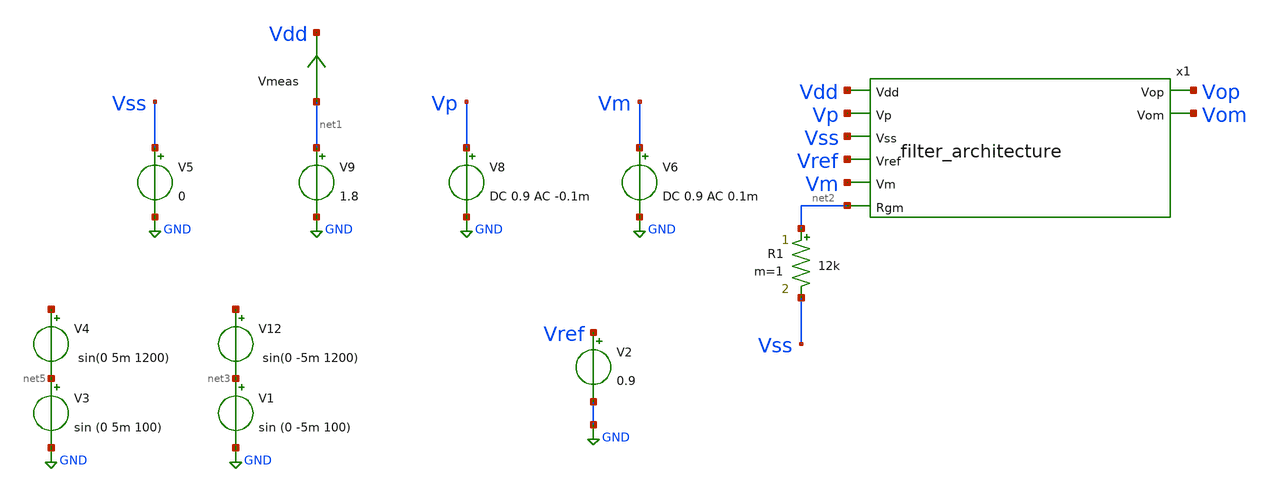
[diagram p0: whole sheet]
** sch_path: src/Bandpass_filter/testbenches/Bandpass_filter_tb.sch
**.subckt Bandpass_filter_tb
x1 Vdd Vop Vp Vss Vref Vm Vom net2 filter_architecture
V8 Vp GND DC 0.9 AC -0.1m
V6 Vm GND DC 0.9 AC 0.1m
V9 net1 GND 1.8
Vmeas net1 Vdd 0
.save i(vmeas)
V1 net3 GND sin (0 -5m 100)
V12 net4 net3 sin(0 -5m 1200)
V5 Vss GND 0
R1 net2 Vss 12k m=1
V3 net5 GND sin (0 5m 100)
V4 net6 net5 sin(0 5m 1200)
V2 Vref GND 0.9
**** begin user architecture code

** opencircuitdesign pdks install
.lib $::SKYWATER_MODELS/sky130.lib.spice tt


**** end user architecture code
**.ends

* expanding   symbol:  /foss/designs/FYP/Sky130_Design/Bandpass_filter/Src/filter_architecture.sym #
*+ of pins=8
** sym_path: src/Bandpass_filter/Src/filter_architecture.sym
** sch_path: src/Bandpass_filter/Src/filter_architecture.sch
.subckt filter_architecture Vdd Vop Vp Vss Vref Vm Vom Rgm
*.ipin Vdd
*.opin Vop
*.ipin Vss
*.ipin Vref
*.ipin Rgm
*.ipin Vp
*.ipin Vm
*.opin Vom
x1 Rgm Vop1 net2 Vdd Vref Vss Vom1 net4 Opamp_with_bias
C1 net1 net2 10n m=1
C2 net1 Vop1 10n m=1
R1 net2 Vop1 105k m=1
R2 Vm net1 36.5k m=1
R3 net1 Vref 2.37k m=1
C3 net3 net4 10n m=1
C4 net3 Vom1 10n m=1
R4 net4 Vom1 105k m=1
R5 Vp net3 36.5k m=1
R6 net3 Vref 2.37k m=1
x2 Rgm Vop net6 Vdd Vref Vss Vom net8 Opamp_with_bias
C5 net5 net6 10n m=1
C6 net5 Vop 10n m=1
R7 net6 Vop 105k m=1
R9 net5 Vref 2.37k m=1
C7 net7 net8 10n m=1
C8 net7 Vom 10n m=1
R10 net8 Vom 105k m=1
R11 Vom1 net5 36.5k m=1
R12 net7 Vref 2.37k m=1
R8 Vop1 net7 36.5k m=1
.ends


* expanding   symbol:  /foss/designs/FYP/Sky130_Design/Opamp_Design/src/Opamp_with_bias.sym # of
*+ pins=8
** sym_path: src/Opamp_Design/src/Opamp_with_bias.sym
** sch_path: src/Opamp_Design/src/Opamp_with_bias.sch
.subckt Opamp_with_bias Rgm Vop Vm Vdd Vref Vss Vom Vp
*.ipin Vdd
*.ipin Vss
*.opin Vop
*.opin Vom
*.ipin Vm
*.ipin Vp
*.ipin Vref
*.ipin Rgm
XM32 NBias PBias Vdd Vdd sky130_fd_pr__pfet_01v8_lvt L=1 W=5 nf=1 ad='int((nf+1)/2) * W/nf * 0.29' as='int((nf+2)/2) * W/nf * 0.29'
+ pd='2*int((nf+1)/2) * (W/nf + 0.29)' ps='2*int((nf+2)/2) * (W/nf + 0.29)' nrd='0.29 / W' nrs='0.29 / W'
+ sa=0 sb=0 sd=0 mult=2 m=2
XM33 NBias NBias Vss Vss sky130_fd_pr__nfet_01v8_lvt L=2 W=5 nf=1 ad='int((nf+1)/2) * W/nf * 0.29' as='int((nf+2)/2) * W/nf * 0.29'
+ pd='2*int((nf+1)/2) * (W/nf + 0.29)' ps='2*int((nf+2)/2) * (W/nf + 0.29)' nrd='0.29 / W' nrs='0.29 / W'
+ sa=0 sb=0 sd=0 mult=2 m=2
XM34 net1 PBias Vdd Vdd sky130_fd_pr__pfet_01v8_lvt L=1 W=5 nf=1 ad='int((nf+1)/2) * W/nf * 0.29' as='int((nf+2)/2) * W/nf * 0.29'
+ pd='2*int((nf+1)/2) * (W/nf + 0.29)' ps='2*int((nf+2)/2) * (W/nf + 0.29)' nrd='0.29 / W' nrs='0.29 / W'
+ sa=0 sb=0 sd=0 mult=2 m=2
XM35 net1 net1 Rgm Vss sky130_fd_pr__nfet_01v8_lvt L=1 W=10 nf=1 ad='int((nf+1)/2) * W/nf * 0.29' as='int((nf+2)/2) * W/nf * 0.29'
+ pd='2*int((nf+1)/2) * (W/nf + 0.29)' ps='2*int((nf+2)/2) * (W/nf + 0.29)' nrd='0.29 / W' nrs='0.29 / W'
+ sa=0 sb=0 sd=0 mult=2 m=2
XM36 net2 net1 Vss Vss sky130_fd_pr__nfet_01v8_lvt L=2 W=5 nf=1 ad='int((nf+1)/2) * W/nf * 0.29' as='int((nf+2)/2) * W/nf * 0.29'
+ pd='2*int((nf+1)/2) * (W/nf + 0.29)' ps='2*int((nf+2)/2) * (W/nf + 0.29)' nrd='0.29 / W' nrs='0.29 / W'
+ sa=0 sb=0 sd=0 mult=2 m=2
XM37 PBias NBias Vss Vss sky130_fd_pr__nfet_01v8_lvt L=2 W=5 nf=1 ad='int((nf+1)/2) * W/nf * 0.29' as='int((nf+2)/2) * W/nf * 0.29'
+ pd='2*int((nf+1)/2) * (W/nf + 0.29)' ps='2*int((nf+2)/2) * (W/nf + 0.29)' nrd='0.29 / W' nrs='0.29 / W'
+ sa=0 sb=0 sd=0 mult=2 m=2
XM38 PBias net2 Vdd Vdd sky130_fd_pr__pfet_01v8_lvt L=1 W=5 nf=1 ad='int((nf+1)/2) * W/nf * 0.29' as='int((nf+2)/2) * W/nf * 0.29'
+ pd='2*int((nf+1)/2) * (W/nf + 0.29)' ps='2*int((nf+2)/2) * (W/nf + 0.29)' nrd='0.29 / W' nrs='0.29 / W'
+ sa=0 sb=0 sd=0 mult=2 m=2
XM39 net2 net2 Vdd Vdd sky130_fd_pr__pfet_01v8_lvt L=1 W=5 nf=1 ad='int((nf+1)/2) * W/nf * 0.29' as='int((nf+2)/2) * W/nf * 0.29'
+ pd='2*int((nf+1)/2) * (W/nf + 0.29)' ps='2*int((nf+2)/2) * (W/nf + 0.29)' nrd='0.29 / W' nrs='0.29 / W'
+ sa=0 sb=0 sd=0 mult=2 m=2
XM40 PBias net3 NBias Vss sky130_fd_pr__nfet_01v8_lvt L=1 W=2 nf=1 ad='int((nf+1)/2) * W/nf * 0.29' as='int((nf+2)/2) * W/nf * 0.29'
+ pd='2*int((nf+1)/2) * (W/nf + 0.29)' ps='2*int((nf+2)/2) * (W/nf + 0.29)' nrd='0.29 / W' nrs='0.29 / W'
+ sa=0 sb=0 sd=0 mult=1 m=1
XM41 net3 NBias Vss Vss sky130_fd_pr__nfet_01v8_lvt L=2 W=5 nf=1 ad='int((nf+1)/2) * W/nf * 0.29' as='int((nf+2)/2) * W/nf * 0.29'
+ pd='2*int((nf+1)/2) * (W/nf + 0.29)' ps='2*int((nf+2)/2) * (W/nf + 0.29)' nrd='0.29 / W' nrs='0.29 / W'
+ sa=0 sb=0 sd=0 mult=2 m=2
XM42 net3 net3 Vdd Vdd sky130_fd_pr__pfet_01v8_lvt L=20 W=1 nf=1 ad='int((nf+1)/2) * W/nf * 0.29' as='int((nf+2)/2) * W/nf * 0.29'
+ pd='2*int((nf+1)/2) * (W/nf + 0.29)' ps='2*int((nf+2)/2) * (W/nf + 0.29)' nrd='0.29 / W' nrs='0.29 / W'
+ sa=0 sb=0 sd=0 mult=2 m=2
XM43 net4 PBias Vdd Vdd sky130_fd_pr__pfet_01v8_lvt L=1 W=5 nf=1 ad='int((nf+1)/2) * W/nf * 0.29' as='int((nf+2)/2) * W/nf * 0.29'
+ pd='2*int((nf+1)/2) * (W/nf + 0.29)' ps='2*int((nf+2)/2) * (W/nf + 0.29)' nrd='0.29 / W' nrs='0.29 / W'
+ sa=0 sb=0 sd=0 mult=2 m=2
XM44 net5 PBias Vdd Vdd sky130_fd_pr__pfet_01v8_lvt L=1 W=5 nf=1 ad='int((nf+1)/2) * W/nf * 0.29' as='int((nf+2)/2) * W/nf * 0.29'
+ pd='2*int((nf+1)/2) * (W/nf + 0.29)' ps='2*int((nf+2)/2) * (W/nf + 0.29)' nrd='0.29 / W' nrs='0.29 / W'
+ sa=0 sb=0 sd=0 mult=2 m=2
XM45 net6 PBias Vdd Vdd sky130_fd_pr__pfet_01v8_lvt L=1 W=5 nf=1 ad='int((nf+1)/2) * W/nf * 0.29' as='int((nf+2)/2) * W/nf * 0.29'
+ pd='2*int((nf+1)/2) * (W/nf + 0.29)' ps='2*int((nf+2)/2) * (W/nf + 0.29)' nrd='0.29 / W' nrs='0.29 / W'
+ sa=0 sb=0 sd=0 mult=2 m=2
XM54 net7 PBias Vdd Vdd sky130_fd_pr__pfet_01v8_lvt L=1 W=5 nf=1 ad='int((nf+1)/2) * W/nf * 0.29' as='int((nf+2)/2) * W/nf * 0.29'
+ pd='2*int((nf+1)/2) * (W/nf + 0.29)' ps='2*int((nf+2)/2) * (W/nf + 0.29)' nrd='0.29 / W' nrs='0.29 / W'
+ sa=0 sb=0 sd=0 mult=2 m=2
XC1 Vop1 Vom sky130_fd_pr__cap_mim_m3_1 W=10 L=10 MF=5 m=5
XC2 Vom1 Vop sky130_fd_pr__cap_mim_m3_1 W=10 L=10 MF=5 m=5
x1 net6 net5 net4 Vm Vp Vss Vdd Vref Vop1 Vom1 Diff_opamp
x2 Vref net7 Vop1 Vom1 Vss Vdd Vop Vom Common_source_stage
.ends


* expanding   symbol:  /foss/designs/FYP/Sky130_Design/Opamp_Design/src/Diff_opamp.sym # of pins=10
** sym_path: src/Opamp_Design/src/Diff_opamp.sym
** sch_path: src/Opamp_Design/src/Diff_opamp.sch
.subckt Diff_opamp Vbias3 Vbias2 Vbias1 Vm Vp Vss Vdd Vref Vop Vom
*.ipin Vss
*.opin Vop
*.ipin Vdd
*.ipin Vp
*.ipin Vm
*.ipin Vref
*.opin Vom
*.ipin Vbias1
*.ipin Vbias2
*.ipin Vbias3
XM5 Vtest2 Vm net2 Vss sky130_fd_pr__nfet_01v8_lvt L=4 W=4 nf=1 ad='int((nf+1)/2) * W/nf * 0.29' as='int((nf+2)/2) * W/nf * 0.29'
+ pd='2*int((nf+1)/2) * (W/nf + 0.29)' ps='2*int((nf+2)/2) * (W/nf + 0.29)' nrd='0.29 / W' nrs='0.29 / W'
+ sa=0 sb=0 sd=0 mult=2 m=2
XM6 net1 Vp net2 Vss sky130_fd_pr__nfet_01v8_lvt L=4 W=4 nf=1 ad='int((nf+1)/2) * W/nf * 0.29' as='int((nf+2)/2) * W/nf * 0.29'
+ pd='2*int((nf+1)/2) * (W/nf + 0.29)' ps='2*int((nf+2)/2) * (W/nf + 0.29)' nrd='0.29 / W' nrs='0.29 / W'
+ sa=0 sb=0 sd=0 mult=2 m=2
XM11 Vop Vbias Vtest2 Vdd sky130_fd_pr__pfet_01v8_lvt L=5 W=2 nf=1 ad='int((nf+1)/2) * W/nf * 0.29' as='int((nf+2)/2) * W/nf * 0.29'
+ pd='2*int((nf+1)/2) * (W/nf + 0.29)' ps='2*int((nf+2)/2) * (W/nf + 0.29)' nrd='0.29 / W' nrs='0.29 / W'
+ sa=0 sb=0 sd=0 mult=2 m=2
XM12 Vom Vbias net1 Vdd sky130_fd_pr__pfet_01v8_lvt L=5 W=2 nf=1 ad='int((nf+1)/2) * W/nf * 0.29' as='int((nf+2)/2) * W/nf * 0.29'
+ pd='2*int((nf+1)/2) * (W/nf + 0.29)' ps='2*int((nf+2)/2) * (W/nf + 0.29)' nrd='0.29 / W' nrs='0.29 / W'
+ sa=0 sb=0 sd=0 mult=2 m=2
XM13 Vtest2 Vout Vdd Vdd sky130_fd_pr__pfet_01v8_lvt L=5 W=2 nf=1 ad='int((nf+1)/2) * W/nf * 0.29' as='int((nf+2)/2) * W/nf * 0.29'
+ pd='2*int((nf+1)/2) * (W/nf + 0.29)' ps='2*int((nf+2)/2) * (W/nf + 0.29)' nrd='0.29 / W' nrs='0.29 / W'
+ sa=0 sb=0 sd=0 mult=4 m=4
XM14 net1 Vout Vdd Vdd sky130_fd_pr__pfet_01v8_lvt L=5 W=2 nf=1 ad='int((nf+1)/2) * W/nf * 0.29' as='int((nf+2)/2) * W/nf * 0.29'
+ pd='2*int((nf+1)/2) * (W/nf + 0.29)' ps='2*int((nf+2)/2) * (W/nf + 0.29)' nrd='0.29 / W' nrs='0.29 / W'
+ sa=0 sb=0 sd=0 mult=4 m=4
XM19 net2 Vbias2 net3 Vss sky130_fd_pr__nfet_01v8_lvt L=1 W=1 nf=1 ad='int((nf+1)/2) * W/nf * 0.29' as='int((nf+2)/2) * W/nf * 0.29'
+ pd='2*int((nf+1)/2) * (W/nf + 0.29)' ps='2*int((nf+2)/2) * (W/nf + 0.29)' nrd='0.29 / W' nrs='0.29 / W'
+ sa=0 sb=0 sd=0 mult=2 m=2
XM1 net3 Vbias1 Vss Vss sky130_fd_pr__nfet_01v8_lvt L=10 W=1 nf=1 ad='int((nf+1)/2) * W/nf * 0.29' as='int((nf+2)/2) * W/nf * 0.29'
+ pd='2*int((nf+1)/2) * (W/nf + 0.29)' ps='2*int((nf+2)/2) * (W/nf + 0.29)' nrd='0.29 / W' nrs='0.29 / W'
+ sa=0 sb=0 sd=0 mult=2 m=2
XM2 net4 Vbias1 Vss Vss sky130_fd_pr__nfet_01v8_lvt L=10 W=1 nf=1 ad='int((nf+1)/2) * W/nf * 0.29' as='int((nf+2)/2) * W/nf * 0.29'
+ pd='2*int((nf+1)/2) * (W/nf + 0.29)' ps='2*int((nf+2)/2) * (W/nf + 0.29)' nrd='0.29 / W' nrs='0.29 / W'
+ sa=0 sb=0 sd=0 mult=2 m=2
XM3 net2 Vbias2 net4 Vss sky130_fd_pr__nfet_01v8_lvt L=1 W=1 nf=1 ad='int((nf+1)/2) * W/nf * 0.29' as='int((nf+2)/2) * W/nf * 0.29'
+ pd='2*int((nf+1)/2) * (W/nf + 0.29)' ps='2*int((nf+2)/2) * (W/nf + 0.29)' nrd='0.29 / W' nrs='0.29 / W'
+ sa=0 sb=0 sd=0 mult=2 m=2
XM4 Vop Vbias2 net5 Vss sky130_fd_pr__nfet_01v8_lvt L=1 W=1 nf=1 ad='int((nf+1)/2) * W/nf * 0.29' as='int((nf+2)/2) * W/nf * 0.29'
+ pd='2*int((nf+1)/2) * (W/nf + 0.29)' ps='2*int((nf+2)/2) * (W/nf + 0.29)' nrd='0.29 / W' nrs='0.29 / W'
+ sa=0 sb=0 sd=0 mult=2 m=2
XM7 net5 Vbias1 Vss Vss sky130_fd_pr__nfet_01v8_lvt L=10 W=1 nf=1 ad='int((nf+1)/2) * W/nf * 0.29' as='int((nf+2)/2) * W/nf * 0.29'
+ pd='2*int((nf+1)/2) * (W/nf + 0.29)' ps='2*int((nf+2)/2) * (W/nf + 0.29)' nrd='0.29 / W' nrs='0.29 / W'
+ sa=0 sb=0 sd=0 mult=2 m=2
XM8 Vom Vbias2 net6 Vss sky130_fd_pr__nfet_01v8_lvt L=1 W=1 nf=1 ad='int((nf+1)/2) * W/nf * 0.29' as='int((nf+2)/2) * W/nf * 0.29'
+ pd='2*int((nf+1)/2) * (W/nf + 0.29)' ps='2*int((nf+2)/2) * (W/nf + 0.29)' nrd='0.29 / W' nrs='0.29 / W'
+ sa=0 sb=0 sd=0 mult=2 m=2
XM9 net6 Vbias1 Vss Vss sky130_fd_pr__nfet_01v8_lvt L=10 W=1 nf=1 ad='int((nf+1)/2) * W/nf * 0.29' as='int((nf+2)/2) * W/nf * 0.29'
+ pd='2*int((nf+1)/2) * (W/nf + 0.29)' ps='2*int((nf+2)/2) * (W/nf + 0.29)' nrd='0.29 / W' nrs='0.29 / W'
+ sa=0 sb=0 sd=0 mult=2 m=2
XM10 Vout Vref net8 Vss sky130_fd_pr__nfet_01v8_lvt L=20 W=5 nf=1 ad='int((nf+1)/2) * W/nf * 0.29' as='int((nf+2)/2) * W/nf * 0.29'
+ pd='2*int((nf+1)/2) * (W/nf + 0.29)' ps='2*int((nf+2)/2) * (W/nf + 0.29)' nrd='0.29 / W' nrs='0.29 / W'
+ sa=0 sb=0 sd=0 mult=2 m=2
XM17 net9 Vop net8 Vss sky130_fd_pr__nfet_01v8_lvt L=20 W=5 nf=1 ad='int((nf+1)/2) * W/nf * 0.29' as='int((nf+2)/2) * W/nf * 0.29'
+ pd='2*int((nf+1)/2) * (W/nf + 0.29)' ps='2*int((nf+2)/2) * (W/nf + 0.29)' nrd='0.29 / W' nrs='0.29 / W'
+ sa=0 sb=0 sd=0 mult=2 m=2
XM18 net9 Vom net7 Vss sky130_fd_pr__nfet_01v8_lvt L=20 W=5 nf=1 ad='int((nf+1)/2) * W/nf * 0.29' as='int((nf+2)/2) * W/nf * 0.29'
+ pd='2*int((nf+1)/2) * (W/nf + 0.29)' ps='2*int((nf+2)/2) * (W/nf + 0.29)' nrd='0.29 / W' nrs='0.29 / W'
+ sa=0 sb=0 sd=0 mult=2 m=2
XM22 net7 Vbias1 Vss Vss sky130_fd_pr__nfet_01v8_lvt L=20 W=1 nf=1 ad='int((nf+1)/2) * W/nf * 0.29' as='int((nf+2)/2) * W/nf * 0.29'
+ pd='2*int((nf+1)/2) * (W/nf + 0.29)' ps='2*int((nf+2)/2) * (W/nf + 0.29)' nrd='0.29 / W' nrs='0.29 / W'
+ sa=0 sb=0 sd=0 mult=2 m=2
XM20 net9 net9 Vdd Vdd sky130_fd_pr__pfet_01v8_lvt L=10 W=1 nf=1 ad='int((nf+1)/2) * W/nf * 0.29' as='int((nf+2)/2) * W/nf * 0.29'
+ pd='2*int((nf+1)/2) * (W/nf + 0.29)' ps='2*int((nf+2)/2) * (W/nf + 0.29)' nrd='0.29 / W' nrs='0.29 / W'
+ sa=0 sb=0 sd=0 mult=2 m=2
XM21 Vout net9 Vdd Vdd sky130_fd_pr__pfet_01v8_lvt L=10 W=1 nf=1 ad='int((nf+1)/2) * W/nf * 0.29' as='int((nf+2)/2) * W/nf * 0.29'
+ pd='2*int((nf+1)/2) * (W/nf + 0.29)' ps='2*int((nf+2)/2) * (W/nf + 0.29)' nrd='0.29 / W' nrs='0.29 / W'
+ sa=0 sb=0 sd=0 mult=2 m=2
XM15 net8 Vbias1 Vss Vss sky130_fd_pr__nfet_01v8_lvt L=20 W=1 nf=1 ad='int((nf+1)/2) * W/nf * 0.29' as='int((nf+2)/2) * W/nf * 0.29'
+ pd='2*int((nf+1)/2) * (W/nf + 0.29)' ps='2*int((nf+2)/2) * (W/nf + 0.29)' nrd='0.29 / W' nrs='0.29 / W'
+ sa=0 sb=0 sd=0 mult=2 m=2
XM16 Vout Vref net7 Vss sky130_fd_pr__nfet_01v8_lvt L=20 W=5 nf=1 ad='int((nf+1)/2) * W/nf * 0.29' as='int((nf+2)/2) * W/nf * 0.29'
+ pd='2*int((nf+1)/2) * (W/nf + 0.29)' ps='2*int((nf+2)/2) * (W/nf + 0.29)' nrd='0.29 / W' nrs='0.29 / W'
+ sa=0 sb=0 sd=0 mult=2 m=2
XM46 Vbias1 Vbias1 Vss Vss sky130_fd_pr__nfet_01v8_lvt L=2 W=1 nf=1 ad='int((nf+1)/2) * W/nf * 0.29'
+ as='int((nf+2)/2) * W/nf * 0.29' pd='2*int((nf+1)/2) * (W/nf + 0.29)' ps='2*int((nf+2)/2) * (W/nf + 0.29)'
+ nrd='0.29 / W' nrs='0.29 / W' sa=0 sb=0 sd=0 mult=2 m=2
XM47 Vbias2 Vbias2 Vss Vss sky130_fd_pr__nfet_01v8_lvt L=5 W=0.6 nf=1 ad='int((nf+1)/2) * W/nf * 0.29'
+ as='int((nf+2)/2) * W/nf * 0.29' pd='2*int((nf+1)/2) * (W/nf + 0.29)' ps='2*int((nf+2)/2) * (W/nf + 0.29)'
+ nrd='0.29 / W' nrs='0.29 / W' sa=0 sb=0 sd=0 mult=2 m=2
XM23 Vbias3 Vbias3 Vss Vss sky130_fd_pr__nfet_01v8_lvt L=1 W=0.6 nf=1 ad='int((nf+1)/2) * W/nf * 0.29'
+ as='int((nf+2)/2) * W/nf * 0.29' pd='2*int((nf+1)/2) * (W/nf + 0.29)' ps='2*int((nf+2)/2) * (W/nf + 0.29)'
+ nrd='0.29 / W' nrs='0.29 / W' sa=0 sb=0 sd=0 mult=2 m=2
XM24 Vbias Vbias3 Vss Vss sky130_fd_pr__nfet_01v8_lvt L=1 W=0.6 nf=1 ad='int((nf+1)/2) * W/nf * 0.29'
+ as='int((nf+2)/2) * W/nf * 0.29' pd='2*int((nf+1)/2) * (W/nf + 0.29)' ps='2*int((nf+2)/2) * (W/nf + 0.29)'
+ nrd='0.29 / W' nrs='0.29 / W' sa=0 sb=0 sd=0 mult=2 m=2
XM25 Vbias Vbias Vdd Vdd sky130_fd_pr__pfet_01v8_lvt L=10 W=1.5 nf=1 ad='int((nf+1)/2) * W/nf * 0.29'
+ as='int((nf+2)/2) * W/nf * 0.29' pd='2*int((nf+1)/2) * (W/nf + 0.29)' ps='2*int((nf+2)/2) * (W/nf + 0.29)'
+ nrd='0.29 / W' nrs='0.29 / W' sa=0 sb=0 sd=0 mult=2 m=2
.ends


* expanding   symbol:  /foss/designs/FYP/Sky130_Design/Opamp_Design/src/Common_source_stage.sym # of
*+ pins=8
** sym_path: src/Opamp_Design/src/Common_source_stage.sym
** sch_path: src/Opamp_Design/src/Common_source_stage.sch
.subckt Common_source_stage Vref Vbias Vomin Vopin Vss Vdd Vop Vom
*.ipin Vdd
*.opin Vop
*.ipin Vss
*.opin Vom
*.ipin Vopin
*.ipin Vomin
*.ipin Vbias
*.ipin Vref
XM9 Vop Vopin Vdd Vdd sky130_fd_pr__pfet_01v8_lvt L=1 W=2 nf=1 ad='int((nf+1)/2) * W/nf * 0.29' as='int((nf+2)/2) * W/nf * 0.29'
+ pd='2*int((nf+1)/2) * (W/nf + 0.29)' ps='2*int((nf+2)/2) * (W/nf + 0.29)' nrd='0.29 / W' nrs='0.29 / W'
+ sa=0 sb=0 sd=0 mult=9 m=9
XM4 Vom Vomin Vdd Vdd sky130_fd_pr__pfet_01v8_lvt L=1 W=2 nf=1 ad='int((nf+1)/2) * W/nf * 0.29' as='int((nf+2)/2) * W/nf * 0.29'
+ pd='2*int((nf+1)/2) * (W/nf + 0.29)' ps='2*int((nf+2)/2) * (W/nf + 0.29)' nrd='0.29 / W' nrs='0.29 / W'
+ sa=0 sb=0 sd=0 mult=9 m=9
XM2 Vop Vout Vss Vss sky130_fd_pr__nfet_01v8_lvt L=1 W=1 nf=1 ad='int((nf+1)/2) * W/nf * 0.29' as='int((nf+2)/2) * W/nf * 0.29'
+ pd='2*int((nf+1)/2) * (W/nf + 0.29)' ps='2*int((nf+2)/2) * (W/nf + 0.29)' nrd='0.29 / W' nrs='0.29 / W'
+ sa=0 sb=0 sd=0 mult=9 m=9
XM1 Vom Vout Vss Vss sky130_fd_pr__nfet_01v8_lvt L=1 W=1 nf=1 ad='int((nf+1)/2) * W/nf * 0.29' as='int((nf+2)/2) * W/nf * 0.29'
+ pd='2*int((nf+1)/2) * (W/nf + 0.29)' ps='2*int((nf+2)/2) * (W/nf + 0.29)' nrd='0.29 / W' nrs='0.29 / W'
+ sa=0 sb=0 sd=0 mult=9 m=9
XM3 net1 Vbiasp Vdd Vdd sky130_fd_pr__pfet_01v8_lvt L=5 W=1 nf=1 ad='int((nf+1)/2) * W/nf * 0.29' as='int((nf+2)/2) * W/nf * 0.29'
+ pd='2*int((nf+1)/2) * (W/nf + 0.29)' ps='2*int((nf+2)/2) * (W/nf + 0.29)' nrd='0.29 / W' nrs='0.29 / W'
+ sa=0 sb=0 sd=0 mult=2 m=2
XM7 Vtest Vcm net1 Vdd sky130_fd_pr__pfet_01v8_lvt L=10 W=1 nf=1 ad='int((nf+1)/2) * W/nf * 0.29' as='int((nf+2)/2) * W/nf * 0.29'
+ pd='2*int((nf+1)/2) * (W/nf + 0.29)' ps='2*int((nf+2)/2) * (W/nf + 0.29)' nrd='0.29 / W' nrs='0.29 / W'
+ sa=0 sb=0 sd=0 mult=2 m=2
XM8 Vout Vref net1 Vdd sky130_fd_pr__pfet_01v8_lvt L=10 W=1 nf=1 ad='int((nf+1)/2) * W/nf * 0.29' as='int((nf+2)/2) * W/nf * 0.29'
+ pd='2*int((nf+1)/2) * (W/nf + 0.29)' ps='2*int((nf+2)/2) * (W/nf + 0.29)' nrd='0.29 / W' nrs='0.29 / W'
+ sa=0 sb=0 sd=0 mult=2 m=2
XM5 Vtest Vtest Vss Vss sky130_fd_pr__nfet_01v8_lvt L=20 W=0.5 nf=1 ad='int((nf+1)/2) * W/nf * 0.29'
+ as='int((nf+2)/2) * W/nf * 0.29' pd='2*int((nf+1)/2) * (W/nf + 0.29)' ps='2*int((nf+2)/2) * (W/nf + 0.29)'
+ nrd='0.29 / W' nrs='0.29 / W' sa=0 sb=0 sd=0 mult=2 m=2
XM6 Vout Vtest Vss Vss sky130_fd_pr__nfet_01v8_lvt L=20 W=0.5 nf=1 ad='int((nf+1)/2) * W/nf * 0.29' as='int((nf+2)/2) * W/nf * 0.29'
+ pd='2*int((nf+1)/2) * (W/nf + 0.29)' ps='2*int((nf+2)/2) * (W/nf + 0.29)' nrd='0.29 / W' nrs='0.29 / W'
+ sa=0 sb=0 sd=0 mult=2 m=2
x1 Vop Vcm res_pack
x2 Vcm Vom res_pack
XM10 Vbias Vbias Vss Vss sky130_fd_pr__nfet_01v8_lvt L=1 W=0.6 nf=1 ad='int((nf+1)/2) * W/nf * 0.29'
+ as='int((nf+2)/2) * W/nf * 0.29' pd='2*int((nf+1)/2) * (W/nf + 0.29)' ps='2*int((nf+2)/2) * (W/nf + 0.29)'
+ nrd='0.29 / W' nrs='0.29 / W' sa=0 sb=0 sd=0 mult=2 m=2
XM11 Vbiasp Vbias Vss Vss sky130_fd_pr__nfet_01v8_lvt L=1 W=0.6 nf=1 ad='int((nf+1)/2) * W/nf * 0.29'
+ as='int((nf+2)/2) * W/nf * 0.29' pd='2*int((nf+1)/2) * (W/nf + 0.29)' ps='2*int((nf+2)/2) * (W/nf + 0.29)'
+ nrd='0.29 / W' nrs='0.29 / W' sa=0 sb=0 sd=0 mult=2 m=2
XM12 Vbiasp Vbiasp Vdd Vdd sky130_fd_pr__pfet_01v8_lvt L=1 W=6 nf=1 ad='int((nf+1)/2) * W/nf * 0.29'
+ as='int((nf+2)/2) * W/nf * 0.29' pd='2*int((nf+1)/2) * (W/nf + 0.29)' ps='2*int((nf+2)/2) * (W/nf + 0.29)'
+ nrd='0.29 / W' nrs='0.29 / W' sa=0 sb=0 sd=0 mult=2 m=2
.ends


* expanding   symbol:  /foss/designs/FYP/Sky130_Design/Opamp_Design/src/res_pack.sym # of pins=2
** sym_path: src/Opamp_Design/src/res_pack.sym
** sch_path: src/Opamp_Design/src/res_pack.sch
.subckt res_pack Vin Vout
*.ipin Vin
*.opin Vout
XR1 net4 Vin sky130_fd_pr__res_generic_po W=0.5 L=40 m=1
XR2 net5 net4 sky130_fd_pr__res_generic_po W=0.5 L=40 m=1
XR3 net6 net5 sky130_fd_pr__res_generic_po W=0.5 L=40 m=1
XR4 net7 net6 sky130_fd_pr__res_generic_po W=0.5 L=40 m=1
XR5 net1 net7 sky130_fd_pr__res_generic_po W=0.5 L=40 m=1
XR6 net8 net2 sky130_fd_pr__res_generic_po W=0.5 L=40 m=1
XR7 net9 net8 sky130_fd_pr__res_generic_po W=0.5 L=40 m=1
XR8 net10 net9 sky130_fd_pr__res_generic_po W=0.5 L=40 m=1
XR9 net11 net10 sky130_fd_pr__res_generic_po W=0.5 L=40 m=1
XR10 net1 net11 sky130_fd_pr__res_generic_po W=0.5 L=40 m=1
XR11 net12 net2 sky130_fd_pr__res_generic_po W=0.5 L=40 m=1
XR12 net13 net12 sky130_fd_pr__res_generic_po W=0.5 L=40 m=1
XR13 net14 net13 sky130_fd_pr__res_generic_po W=0.5 L=40 m=1
XR14 net15 net14 sky130_fd_pr__res_generic_po W=0.5 L=40 m=1
XR16 net16 Vout sky130_fd_pr__res_generic_po W=0.5 L=40 m=1
XR17 net17 net16 sky130_fd_pr__res_generic_po W=0.5 L=40 m=1
XR18 net18 net17 sky130_fd_pr__res_generic_po W=0.5 L=40 m=1
XR19 net19 net18 sky130_fd_pr__res_generic_po W=0.5 L=40 m=1
XR20 net3 net19 sky130_fd_pr__res_generic_po W=0.5 L=40 m=1
XR15 net3 net15 sky130_fd_pr__res_generic_po W=0.5 L=40 m=1
.ends

.GLOBAL GND
**** begin user architecture code



* ngspice commands
.options savecurrents

.control
save all
save @m.x1.x2.x1.xm5.msky130_fd_pr__nfet_01v8_lvt[gm]
save @m.x1.x2.x1.xm1.msky130_fd_pr__nfet_01v8_lvt[gm]
save @m.x1.x2.x1.xm2.msky130_fd_pr__nfet_01v8_lvt[gm]
save @m.x1.x2.x1.xm3.msky130_fd_pr__nfet_01v8_lvt[gm]
save @m.x1.x2.x1.xm4.msky130_fd_pr__nfet_01v8_lvt[gm]
save @m.x1.x2.x1.xm6.msky130_fd_pr__nfet_01v8_lvt[gm]
save @m.x1.x2.x1.xm7.msky130_fd_pr__nfet_01v8_lvt[gm]
save @m.x1.x2.x1.xm8.msky130_fd_pr__nfet_01v8_lvt[gm]
save @m.x1.x2.x1.xm9.msky130_fd_pr__nfet_01v8_lvt[gm]
save @m.x1.x2.x1.xm10.msky130_fd_pr__nfet_01v8_lvt[gm]
save @m.x1.x2.x1.xm11.msky130_fd_pr__pfet_01v8_lvt[gm]
save @m.x1.x2.x1.xm12.msky130_fd_pr__pfet_01v8_lvt[gm]
save @m.x1.x2.x1.xm13.msky130_fd_pr__pfet_01v8_lvt[gm]
save @m.x1.x2.x1.xm14.msky130_fd_pr__pfet_01v8_lvt[gm]
save @m.x1.x2.x1.xm15.msky130_fd_pr__nfet_01v8_lvt[gm]
save @m.x1.x2.x1.xm16.msky130_fd_pr__nfet_01v8_lvt[gm]
save @m.x1.x2.x1.xm17.msky130_fd_pr__nfet_01v8_lvt[gm]
save @m.x1.x2.x1.xm18.msky130_fd_pr__nfet_01v8_lvt[gm]
save @m.x1.x2.x1.xm19.msky130_fd_pr__nfet_01v8_lvt[gm]
save @m.x1.x2.x1.xm20.msky130_fd_pr__pfet_01v8_lvt[gm]
save @m.x1.x2.x1.xm21.msky130_fd_pr__pfet_01v8_lvt[gm]
save @m.x1.x2.x1.xm22.msky130_fd_pr__nfet_01v8_lvt[gm]

save @m.x1.x2.x2.xm1.msky130_fd_pr__nfet_01v8_lvt[gm]
save @m.x1.x2.x2.xm2.msky130_fd_pr__nfet_01v8_lvt[gm]
save @m.x1.x2.x2.xm3.msky130_fd_pr__pfet_01v8_lvt[gm]
save @m.x1.x2.x2.xm4.msky130_fd_pr__pfet_01v8_lvt[gm]
save @m.x1.x2.x2.xm5.msky130_fd_pr__nfet_01v8_lvt[gm]
save @m.x1.x2.x2.xm6.msky130_fd_pr__nfet_01v8_lvt[gm]
save @m.x1.x2.x2.xm7.msky130_fd_pr__pfet_01v8_lvt[gm]
save @m.x1.x2.x2.xm8.msky130_fd_pr__pfet_01v8_lvt[gm]
save @m.x1.x2.x2.xm9.msky130_fd_pr__pfet_01v8_lvt[gm]

save @m.x1.x1.xm5.msky130_fd_pr__pfet_01v8_lvt[gm]
save @m.x1.x1.xm1.msky130_fd_pr__pfet_01v8_lvt[gm]
save @m.x1.x1.xm2.msky130_fd_pr__nfet_01v8_lvt[gm]
save @m.x1.x1.xm3.msky130_fd_pr__nfet_01v8_lvt[gm]
save @m.x1.x1.xm4.msky130_fd_pr__nfet_01v8_lvt[gm]
save @m.x1.x1.xm6.msky130_fd_pr__pfet_01v8_lvt[gm]
save @m.x1.x1.xm7.msky130_fd_pr__pfet_01v8_lvt[gm]
save @m.x1.x1.xm8.msky130_fd_pr__pfet_01v8_lvt[gm]
save @m.x1.x1.xm9.msky130_fd_pr__nfet_01v8_lvt[gm]
save @m.x1.x1.xm10.msky130_fd_pr__nfet_01v8_lvt[gm]
save @m.x1.x1.xm11.msky130_fd_pr__pfet_01v8_lvt[gm]
save @m.x1.x1.xm12.msky130_fd_pr__nfet_01v8_lvt[gm]
save @m.x1.x1.xm13.msky130_fd_pr__nfet_01v8_lvt[gm]
save @m.x1.x1.xm14.msky130_fd_pr__nfet_01v8_lvt[gm]
save @m.x1.x1.xm15.msky130_fd_pr__nfet_01v8_lvt[gm]
save @m.x1.x1.xm16.msky130_fd_pr__pfet_01v8_lvt[gm]
save @m.x1.x1.xm17.msky130_fd_pr__pfet_01v8_lvt[gm]
save @m.x1.x1.xm18.msky130_fd_pr__pfet_01v8_lvt[gm]
save @m.x1.x1.xm19.msky130_fd_pr__pfet_01v8_lvt[gm]
save @m.x1.x1.xm20.msky130_fd_pr__nfet_01v8_lvt[gm]
save @m.x1.x1.xm21.msky130_fd_pr__nfet_01v8_lvt[gm]
save @m.x1.x1.xm22.msky130_fd_pr__pfet_01v8_lvt[gm]

save @m.x1.x1.x1.xm1.msky130_fd_pr__pfet_01v8_lvt[gm]
save @m.x1.x1.x1.xm2.msky130_fd_pr__nfet_01v8_lvt[gm]
save @m.x1.x1.x1.xm3.msky130_fd_pr__pfet_01v8_lvt[gm]
save @m.x1.x1.x1.xm4.msky130_fd_pr__nfet_01v8_lvt[gm]
save @m.x1.x1.x1.xm5.msky130_fd_pr__nfet_01v8_lvt[gm]
save @m.x1.x1.x1.xm6.msky130_fd_pr__nfet_01v8_lvt[gm]
save @m.x1.x1.x1.xm7.msky130_fd_pr__pfet_01v8_lvt[gm]
save @m.x1.x1.x1.xm8.msky130_fd_pr__pfet_01v8_lvt[gm]
save @m.x1.x1.x1.xm9.msky130_fd_pr__nfet_01v8_lvt[gm]
save @m.x1.x1.x1.xm10.msky130_fd_pr__nfet_01v8_lvt[gm]
save @m.x1.x1.x1.xm11.msky130_fd_pr__pfet_01v8_lvt[gm]



save @m.x1.x2.x1.xm5.msky130_fd_pr__nfet_01v8_lvt[vth]
save @m.x1.x2.x1.xm1.msky130_fd_pr__nfet_01v8_lvt[vth]
save @m.x1.x2.x1.xm2.msky130_fd_pr__nfet_01v8_lvt[vth]
save @m.x1.x2.x1.xm3.msky130_fd_pr__nfet_01v8_lvt[vth]
save @m.x1.x2.x1.xm4.msky130_fd_pr__nfet_01v8_lvt[vth]
save @m.x1.x2.x1.xm6.msky130_fd_pr__nfet_01v8_lvt[vth]
save @m.x1.x2.x1.xm7.msky130_fd_pr__nfet_01v8_lvt[vth]
save @m.x1.x2.x1.xm8.msky130_fd_pr__nfet_01v8_lvt[vth]
save @m.x1.x2.x1.xm9.msky130_fd_pr__nfet_01v8_lvt[vth]
save @m.x1.x2.x1.xm10.msky130_fd_pr__nfet_01v8_lvt[vth]
save @m.x1.x2.x1.xm11.msky130_fd_pr__pfet_01v8_lvt[vth]
save @m.x1.x2.x1.xm12.msky130_fd_pr__pfet_01v8_lvt[vth]
save @m.x1.x2.x1.xm13.msky130_fd_pr__pfet_01v8_lvt[vth]
save @m.x1.x2.x1.xm14.msky130_fd_pr__pfet_01v8_lvt[vth]
save @m.x1.x2.x1.xm15.msky130_fd_pr__nfet_01v8_lvt[vth]
save @m.x1.x2.x1.xm16.msky130_fd_pr__nfet_01v8_lvt[vth]
save @m.x1.x2.x1.xm17.msky130_fd_pr__nfet_01v8_lvt[vth]
save @m.x1.x2.x1.xm18.msky130_fd_pr__nfet_01v8_lvt[vth]
save @m.x1.x2.x1.xm19.msky130_fd_pr__nfet_01v8_lvt[vth]
save @m.x1.x2.x1.xm20.msky130_fd_pr__pfet_01v8_lvt[vth]
save @m.x1.x2.x1.xm21.msky130_fd_pr__pfet_01v8_lvt[vth]
save @m.x1.x2.x1.xm22.msky130_fd_pr__nfet_01v8_lvt[vth]

save @m.x1.x2.x2.xm1.msky130_fd_pr__nfet_01v8_lvt[vth]
save @m.x1.x2.x2.xm2.msky130_fd_pr__nfet_01v8_lvt[vth]
save @m.x1.x2.x2.xm3.msky130_fd_pr__pfet_01v8_lvt[vth]
save @m.x1.x2.x2.xm4.msky130_fd_pr__pfet_01v8_lvt[vth]
save @m.x1.x2.x2.xm5.msky130_fd_pr__nfet_01v8_lvt[vth]
save @m.x1.x2.x2.xm6.msky130_fd_pr__nfet_01v8_lvt[vth]
save @m.x1.x2.x2.xm7.msky130_fd_pr__pfet_01v8_lvt[vth]
save @m.x1.x2.x2.xm8.msky130_fd_pr__pfet_01v8_lvt[vth]
save @m.x1.x2.x2.xm9.msky130_fd_pr__pfet_01v8_lvt[vth]

save @m.x1.x1.xm5.msky130_fd_pr__pfet_01v8_lvt[vth]
save @m.x1.x1.xm1.msky130_fd_pr__pfet_01v8_lvt[vth]
save @m.x1.x1.xm2.msky130_fd_pr__nfet_01v8_lvt[vth]
save @m.x1.x1.xm3.msky130_fd_pr__nfet_01v8_lvt[vth]
save @m.x1.x1.xm4.msky130_fd_pr__nfet_01v8_lvt[vth]
save @m.x1.x1.xm6.msky130_fd_pr__pfet_01v8_lvt[vth]
save @m.x1.x1.xm7.msky130_fd_pr__pfet_01v8_lvt[vth]
save @m.x1.x1.xm8.msky130_fd_pr__pfet_01v8_lvt[vth]
save @m.x1.x1.xm9.msky130_fd_pr__nfet_01v8_lvt[vth]
save @m.x1.x1.xm10.msky130_fd_pr__nfet_01v8_lvt[vth]
save @m.x1.x1.xm11.msky130_fd_pr__pfet_01v8_lvt[vth]
save @m.x1.x1.xm12.msky130_fd_pr__nfet_01v8_lvt[vth]
save @m.x1.x1.xm13.msky130_fd_pr__nfet_01v8_lvt[vth]
save @m.x1.x1.xm14.msky130_fd_pr__nfet_01v8_lvt[vth]
save @m.x1.x1.xm15.msky130_fd_pr__nfet_01v8_lvt[vth]
save @m.x1.x1.xm16.msky130_fd_pr__pfet_01v8_lvt[vth]
save @m.x1.x1.xm17.msky130_fd_pr__pfet_01v8_lvt[vth]
save @m.x1.x1.xm18.msky130_fd_pr__pfet_01v8_lvt[vth]
save @m.x1.x1.xm19.msky130_fd_pr__pfet_01v8_lvt[vth]
save @m.x1.x1.xm20.msky130_fd_pr__nfet_01v8_lvt[vth]
save @m.x1.x1.xm21.msky130_fd_pr__nfet_01v8_lvt[vth]
save @m.x1.x1.xm22.msky130_fd_pr__nfet_01v8_lvt[vth]

save @m.x1.x1.x1.xm1.msky130_fd_pr__pfet_01v8_lvt[vth]
save @m.x1.x1.x1.xm2.msky130_fd_pr__nfet_01v8_lvt[vth]
save @m.x1.x1.x1.xm3.msky130_fd_pr__pfet_01v8_lvt[vth]
save @m.x1.x1.x1.xm4.msky130_fd_pr__nfet_01v8_lvt[vth]
save @m.x1.x1.x1.xm5.msky130_fd_pr__nfet_01v8_lvt[vth]
save @m.x1.x1.x1.xm6.msky130_fd_pr__nfet_01v8_lvt[vth]
save @m.x1.x1.x1.xm7.msky130_fd_pr__pfet_01v8_lvt[vth]
save @m.x1.x1.x1.xm8.msky130_fd_pr__pfet_01v8_lvt[vth]
save @m.x1.x1.x1.xm9.msky130_fd_pr__nfet_01v8_lvt[vth]
save @m.x1.x1.x1.xm10.msky130_fd_pr__nfet_01v8_lvt[vth]
save @m.x1.x1.x1.xm11.msky130_fd_pr__pfet_01v8_lvt[vth]


op
ac dec 101 100 100K
*tran 10u 10m
let vdiff = v(Vop)-v(Vom)
let vin = v(Vp) - v(Vm)
plot db(vdiff/vin) (180/pi)*phase(vdiff/vin)

write bandpass_filter.raw
.endc



**** end user architecture code
.end
